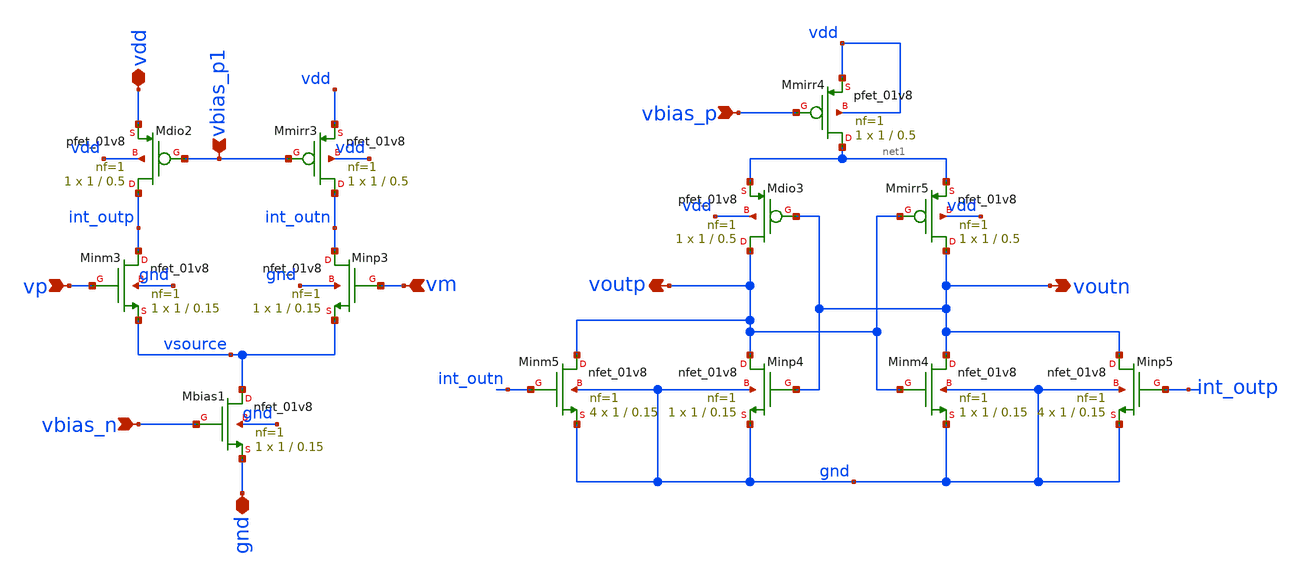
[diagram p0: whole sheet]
** sch_path: analog/xschem/dyn_comp.sch
**.subckt dyn_comp vdd gnd vbias_n vp vm vbias_p voutn voutp vbias_p1
*.iopin vdd
*.iopin gnd
*.ipin vbias_n
*.ipin vp
*.ipin vm
*.ipin vbias_p
*.opin voutn
*.opin voutp
*.ipin vbias_p1
XMmirr3 int_outn vbias_p1 vdd vdd sky130_fd_pr__pfet_01v8 L=0.5 W=1 nf=1 ad='int((1 + 1)/2) * 1 / 1 * 0.29'
+ as='int((1 + 2)/2) * 1 / 1 * 0.29' pd='2*int((1 + 1)/2) * (1 / 1 + 0.29)' ps='2*int((1 + 2)/2) * (1 / 1 + 0.29)'
+ nrd='0.29 / 1 ' nrs='0.29 / 1 ' sa=0 sb=0 sd=0 mult=1 m=1
XMdio2 int_outp vbias_p1 vdd vdd sky130_fd_pr__pfet_01v8 L=0.5 W=1 nf=1 ad='int((1 + 1)/2) * 1 / 1 * 0.29'
+ as='int((1 + 2)/2) * 1 / 1 * 0.29' pd='2*int((1 + 1)/2) * (1 / 1 + 0.29)' ps='2*int((1 + 2)/2) * (1 / 1 + 0.29)'
+ nrd='0.29 / 1 ' nrs='0.29 / 1 ' sa=0 sb=0 sd=0 mult=1 m=1
XMinm3 int_outp vp vsource gnd sky130_fd_pr__nfet_01v8 L=0.15 W=1 nf=1 ad='int((1 + 1)/2) * 1 / 1 * 0.29'
+ as='int((1 + 2)/2) * 1 / 1 * 0.29' pd='2*int((1 + 1)/2) * (1 / 1 + 0.29)' ps='2*int((1 + 2)/2) * (1 / 1 + 0.29)'
+ nrd='0.29 / 1 ' nrs='0.29 / 1 ' sa=0 sb=0 sd=0 mult=1 m=1
XMinp3 int_outn vm vsource gnd sky130_fd_pr__nfet_01v8 L=0.15 W=1 nf=1 ad='int((1 + 1)/2) * 1 / 1 * 0.29'
+ as='int((1 + 2)/2) * 1 / 1 * 0.29' pd='2*int((1 + 1)/2) * (1 / 1 + 0.29)' ps='2*int((1 + 2)/2) * (1 / 1 + 0.29)'
+ nrd='0.29 / 1 ' nrs='0.29 / 1 ' sa=0 sb=0 sd=0 mult=1 m=1
XMbias1 vsource vbias_n gnd gnd sky130_fd_pr__nfet_01v8 L=0.15 W=1 nf=1 ad='int((1 + 1)/2) * 1 / 1 * 0.29'
+ as='int((1 + 2)/2) * 1 / 1 * 0.29' pd='2*int((1 + 1)/2) * (1 / 1 + 0.29)' ps='2*int((1 + 2)/2) * (1 / 1 + 0.29)'
+ nrd='0.29 / 1 ' nrs='0.29 / 1 ' sa=0 sb=0 sd=0 mult=1 m=1
XMmirr4 net1 vbias_p vdd vdd sky130_fd_pr__pfet_01v8 L=0.5 W=1 nf=1 ad='int((1 + 1)/2) * 1 / 1 * 0.29'
+ as='int((1 + 2)/2) * 1 / 1 * 0.29' pd='2*int((1 + 1)/2) * (1 / 1 + 0.29)' ps='2*int((1 + 2)/2) * (1 / 1 + 0.29)'
+ nrd='0.29 / 1 ' nrs='0.29 / 1 ' sa=0 sb=0 sd=0 mult=1 m=1
XMmirr5 voutn voutp net1 vdd sky130_fd_pr__pfet_01v8 L=0.5 W=1 nf=1 ad='int((1 + 1)/2) * 1 / 1 * 0.29'
+ as='int((1 + 2)/2) * 1 / 1 * 0.29' pd='2*int((1 + 1)/2) * (1 / 1 + 0.29)' ps='2*int((1 + 2)/2) * (1 / 1 + 0.29)'
+ nrd='0.29 / 1 ' nrs='0.29 / 1 ' sa=0 sb=0 sd=0 mult=1 m=1
XMdio3 voutp voutn net1 vdd sky130_fd_pr__pfet_01v8 L=0.5 W=1 nf=1 ad='int((1 + 1)/2) * 1 / 1 * 0.29'
+ as='int((1 + 2)/2) * 1 / 1 * 0.29' pd='2*int((1 + 1)/2) * (1 / 1 + 0.29)' ps='2*int((1 + 2)/2) * (1 / 1 + 0.29)'
+ nrd='0.29 / 1 ' nrs='0.29 / 1 ' sa=0 sb=0 sd=0 mult=1 m=1
XMinp4 voutp voutn gnd gnd sky130_fd_pr__nfet_01v8 L=0.15 W=1 nf=1 ad='int((1 + 1)/2) * 1 / 1 * 0.29'
+ as='int((1 + 2)/2) * 1 / 1 * 0.29' pd='2*int((1 + 1)/2) * (1 / 1 + 0.29)' ps='2*int((1 + 2)/2) * (1 / 1 + 0.29)'
+ nrd='0.29 / 1 ' nrs='0.29 / 1 ' sa=0 sb=0 sd=0 mult=1 m=1
XMinm4 voutn voutp gnd gnd sky130_fd_pr__nfet_01v8 L=0.15 W=1 nf=1 ad='int((1 + 1)/2) * 1 / 1 * 0.29'
+ as='int((1 + 2)/2) * 1 / 1 * 0.29' pd='2*int((1 + 1)/2) * (1 / 1 + 0.29)' ps='2*int((1 + 2)/2) * (1 / 1 + 0.29)'
+ nrd='0.29 / 1 ' nrs='0.29 / 1 ' sa=0 sb=0 sd=0 mult=1 m=1
XMinm5 voutp int_outn gnd gnd sky130_fd_pr__nfet_01v8 L=0.15 W=1 nf=1 ad='int((1 + 1)/2) * 1 / 1 * 0.29'
+ as='int((1 + 2)/2) * 1 / 1 * 0.29' pd='2*int((1 + 1)/2) * (1 / 1 + 0.29)' ps='2*int((1 + 2)/2) * (1 / 1 + 0.29)'
+ nrd='0.29 / 1 ' nrs='0.29 / 1 ' sa=0 sb=0 sd=0 mult=4 m=4
XMinp5 voutn int_outp gnd gnd sky130_fd_pr__nfet_01v8 L=0.15 W=1 nf=1 ad='int((1 + 1)/2) * 1 / 1 * 0.29'
+ as='int((1 + 2)/2) * 1 / 1 * 0.29' pd='2*int((1 + 1)/2) * (1 / 1 + 0.29)' ps='2*int((1 + 2)/2) * (1 / 1 + 0.29)'
+ nrd='0.29 / 1 ' nrs='0.29 / 1 ' sa=0 sb=0 sd=0 mult=4 m=4
**.ends
.end
